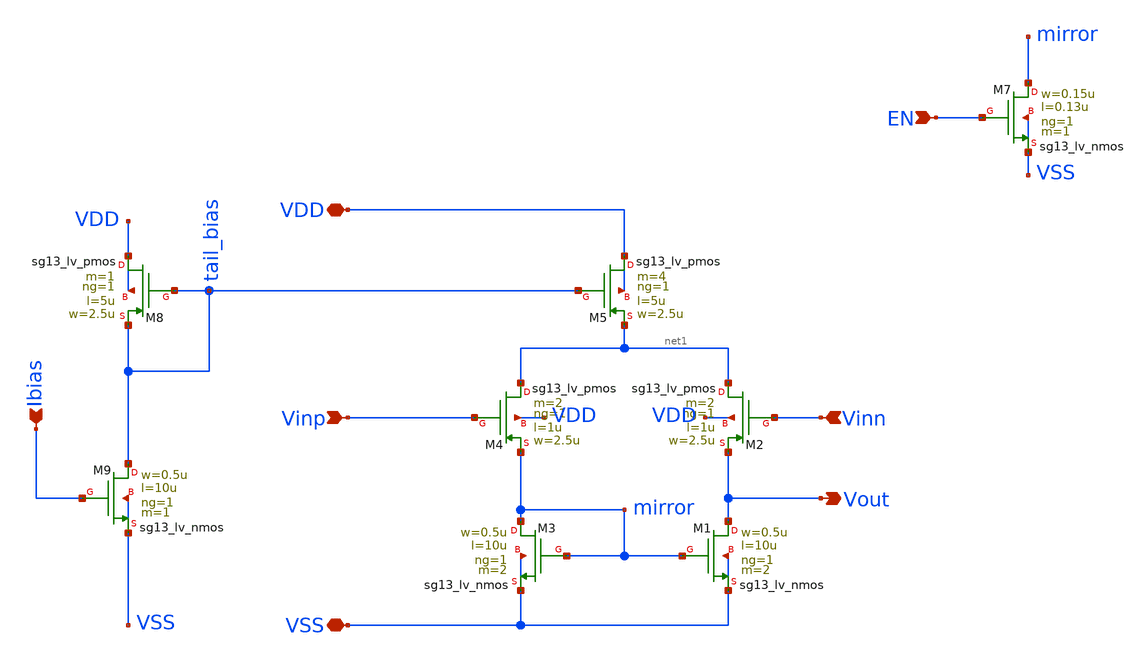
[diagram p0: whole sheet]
** sch_path: schema/ota_cmfb_fbota/ota_cmfb_fbota.sch
**.subckt ota_cmfb_fbota Vout VDD VSS Vinp Ibias Vinn EN
*.opin Vout
*.iopin VDD
*.iopin VSS
*.ipin Vinp
*.ipin Ibias
*.ipin Vinn
*.ipin EN
XM1 Vout mirror VSS VSS sg13_lv_nmos w=0.5u l=10u ng=1 m=2 mm_ok=1
XM2 net1 Vinn Vout VDD sg13_lv_pmos w=2.5u l=1u ng=1 m=2 mm_ok=1
XM3 mirror mirror VSS VSS sg13_lv_nmos w=0.5u l=10u ng=1 m=2 mm_ok=1
XM4 net1 Vinp mirror VDD sg13_lv_pmos w=2.5u l=1u ng=1 m=2 mm_ok=1
XM5 VDD tail_bias net1 VDD sg13_lv_pmos w=2.5u l=5u ng=1 m=4 mm_ok=1
XM7 mirror EN VSS VSS sg13_lv_nmos w=0.15u l=0.13u ng=1 m=1 mm_ok=1
XM8 VDD tail_bias tail_bias VDD sg13_lv_pmos w=2.5u l=5u ng=1 m=1 mm_ok=1
XM9 tail_bias Ibias VSS VSS sg13_lv_nmos w=0.5u l=10u ng=1 m=1 mm_ok=1
**.ends
.end
